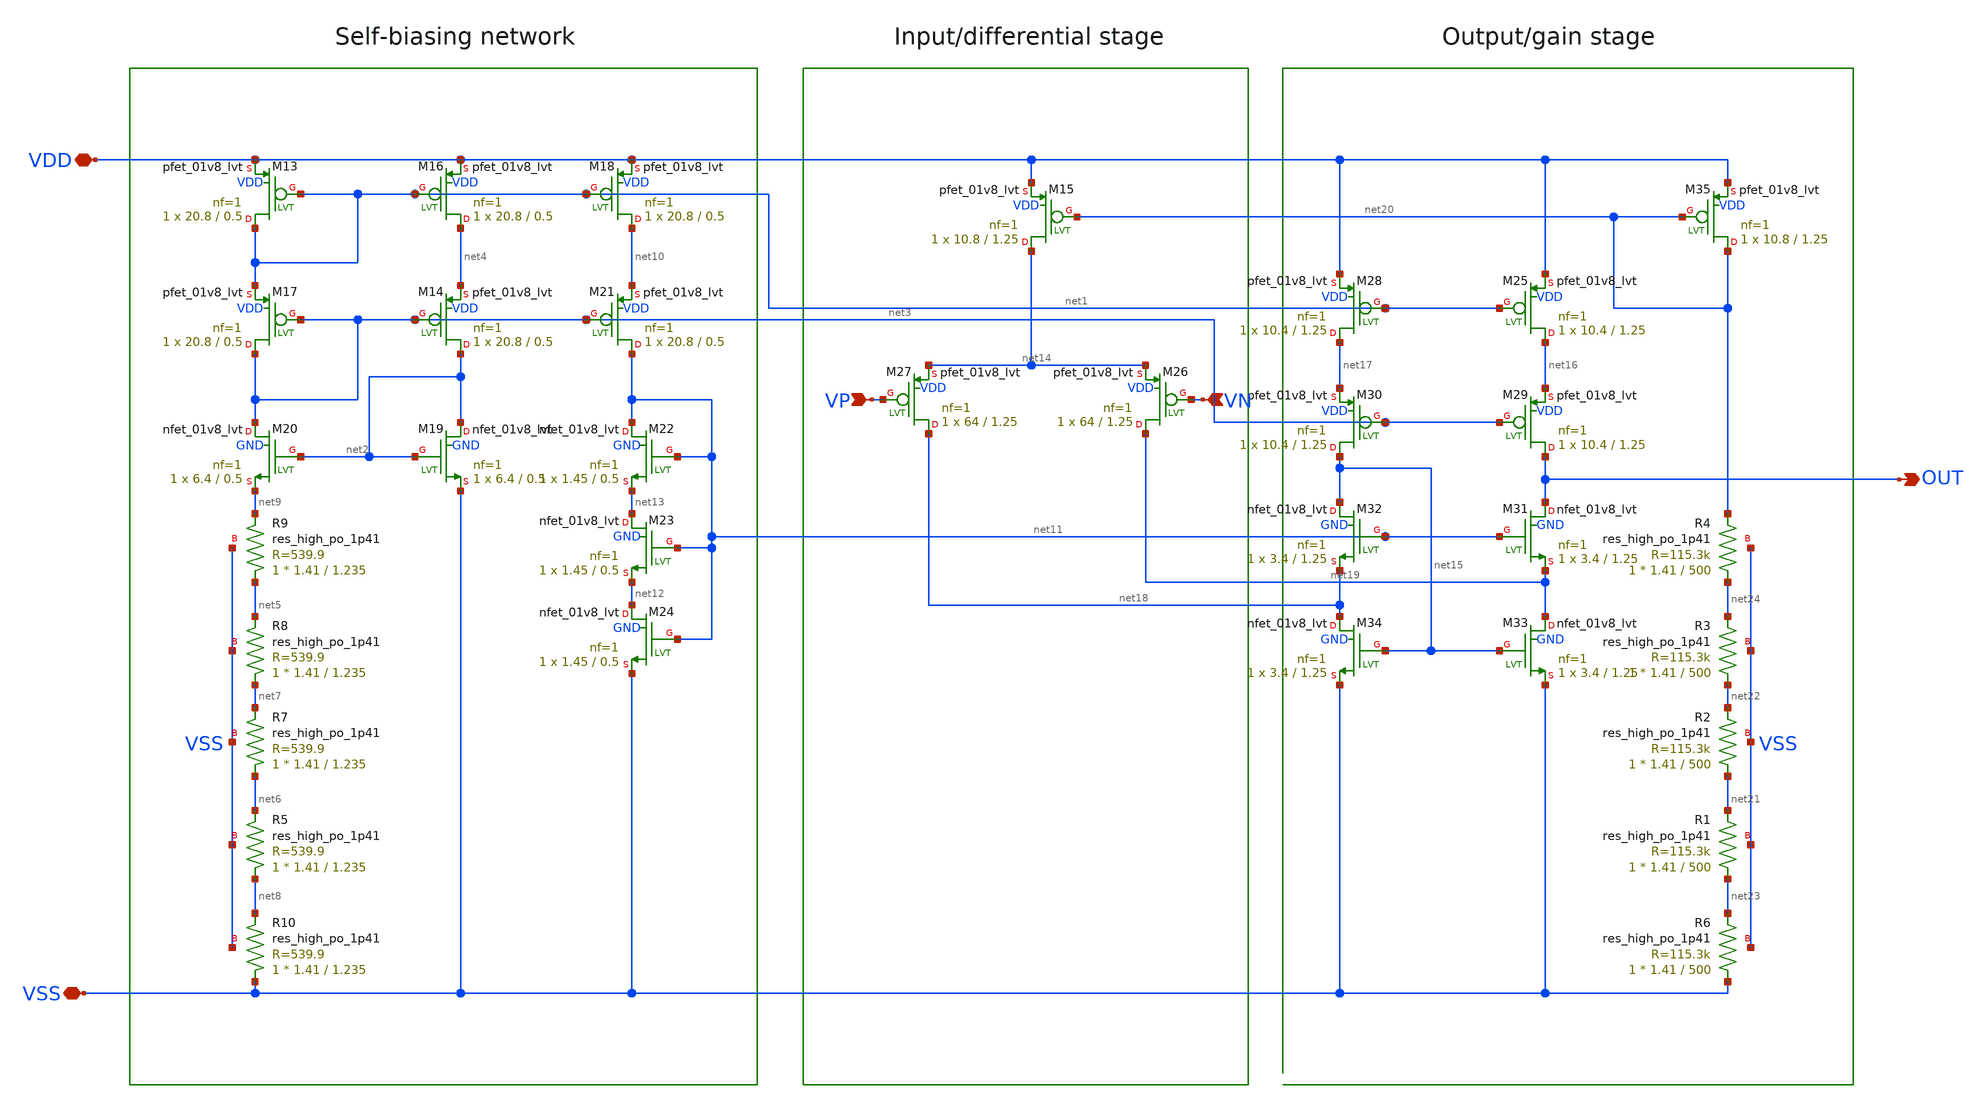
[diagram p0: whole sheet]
** sch_path: bandgap/bgr-opamp2/folded-cascode-opamp.sch
**.subckt folded-cascode-opamp VSS VDD VP VN OUT
*.iopin VSS
*.iopin VDD
*.ipin VP
*.ipin VN
*.opin OUT
XR10 VSS net8 VSS sky130_fd_pr__res_high_po_1p41 L=1.235 mult=1 m=1
XM19 net2 net2 VSS GND sky130_fd_pr__nfet_01v8_lvt L=0.5 W=6.4 nf=1 ad='int((nf+1)/2) * W/nf * 0.29'
+ as='int((nf+2)/2) * W/nf * 0.29' pd='2*int((nf+1)/2) * (W/nf + 0.29)' ps='2*int((nf+2)/2) * (W/nf + 0.29)'
+ nrd='0.29 / W' nrs='0.29 / W' sa=0 sb=0 sd=0 mult=1 m=1
XM20 net3 net2 net9 GND sky130_fd_pr__nfet_01v8_lvt L=0.5 W=6.4 nf=1 ad='int((nf+1)/2) * W/nf * 0.29'
+ as='int((nf+2)/2) * W/nf * 0.29' pd='2*int((nf+1)/2) * (W/nf + 0.29)' ps='2*int((nf+2)/2) * (W/nf + 0.29)'
+ nrd='0.29 / W' nrs='0.29 / W' sa=0 sb=0 sd=0 mult=1 m=1
XM16 net4 net1 VDD VDD sky130_fd_pr__pfet_01v8_lvt L=0.5 W=20.8 nf=1 ad='int((nf+1)/2) * W/nf * 0.29'
+ as='int((nf+2)/2) * W/nf * 0.29' pd='2*int((nf+1)/2) * (W/nf + 0.29)' ps='2*int((nf+2)/2) * (W/nf + 0.29)'
+ nrd='0.29 / W' nrs='0.29 / W' sa=0 sb=0 sd=0 mult=1 m=1
XM13 net1 net1 VDD VDD sky130_fd_pr__pfet_01v8_lvt L=0.5 W=20.8 nf=1 ad='int((nf+1)/2) * W/nf * 0.29'
+ as='int((nf+2)/2) * W/nf * 0.29' pd='2*int((nf+1)/2) * (W/nf + 0.29)' ps='2*int((nf+2)/2) * (W/nf + 0.29)'
+ nrd='0.29 / W' nrs='0.29 / W' sa=0 sb=0 sd=0 mult=1 m=1
XM14 net2 net3 net4 VDD sky130_fd_pr__pfet_01v8_lvt L=0.5 W=20.8 nf=1 ad='int((nf+1)/2) * W/nf * 0.29'
+ as='int((nf+2)/2) * W/nf * 0.29' pd='2*int((nf+1)/2) * (W/nf + 0.29)' ps='2*int((nf+2)/2) * (W/nf + 0.29)'
+ nrd='0.29 / W' nrs='0.29 / W' sa=0 sb=0 sd=0 mult=1 m=1
XM17 net3 net3 net1 VDD sky130_fd_pr__pfet_01v8_lvt L=0.5 W=20.8 nf=1 ad='int((nf+1)/2) * W/nf * 0.29'
+ as='int((nf+2)/2) * W/nf * 0.29' pd='2*int((nf+1)/2) * (W/nf + 0.29)' ps='2*int((nf+2)/2) * (W/nf + 0.29)'
+ nrd='0.29 / W' nrs='0.29 / W' sa=0 sb=0 sd=0 mult=1 m=1
XM18 net10 net1 VDD VDD sky130_fd_pr__pfet_01v8_lvt L=0.5 W=20.8 nf=1 ad='int((nf+1)/2) * W/nf * 0.29'
+ as='int((nf+2)/2) * W/nf * 0.29' pd='2*int((nf+1)/2) * (W/nf + 0.29)' ps='2*int((nf+2)/2) * (W/nf + 0.29)'
+ nrd='0.29 / W' nrs='0.29 / W' sa=0 sb=0 sd=0 mult=1 m=1
XM21 net11 net3 net10 VDD sky130_fd_pr__pfet_01v8_lvt L=0.5 W=20.8 nf=1 ad='int((nf+1)/2) * W/nf * 0.29'
+ as='int((nf+2)/2) * W/nf * 0.29' pd='2*int((nf+1)/2) * (W/nf + 0.29)' ps='2*int((nf+2)/2) * (W/nf + 0.29)'
+ nrd='0.29 / W' nrs='0.29 / W' sa=0 sb=0 sd=0 mult=1 m=1
XM22 net11 net11 net13 GND sky130_fd_pr__nfet_01v8_lvt L=0.5 W=1.45 nf=1 ad='int((nf+1)/2) * W/nf * 0.29'
+ as='int((nf+2)/2) * W/nf * 0.29' pd='2*int((nf+1)/2) * (W/nf + 0.29)' ps='2*int((nf+2)/2) * (W/nf + 0.29)'
+ nrd='0.29 / W' nrs='0.29 / W' sa=0 sb=0 sd=0 mult=1 m=1
XM23 net13 net11 net12 GND sky130_fd_pr__nfet_01v8_lvt L=0.5 W=1.45 nf=1 ad='int((nf+1)/2) * W/nf * 0.29'
+ as='int((nf+2)/2) * W/nf * 0.29' pd='2*int((nf+1)/2) * (W/nf + 0.29)' ps='2*int((nf+2)/2) * (W/nf + 0.29)'
+ nrd='0.29 / W' nrs='0.29 / W' sa=0 sb=0 sd=0 mult=1 m=1
XM24 net12 net11 VSS GND sky130_fd_pr__nfet_01v8_lvt L=0.5 W=1.45 nf=1 ad='int((nf+1)/2) * W/nf * 0.29'
+ as='int((nf+2)/2) * W/nf * 0.29' pd='2*int((nf+1)/2) * (W/nf + 0.29)' ps='2*int((nf+2)/2) * (W/nf + 0.29)'
+ nrd='0.29 / W' nrs='0.29 / W' sa=0 sb=0 sd=0 mult=1 m=1
XM26 net19 VN net14 VDD sky130_fd_pr__pfet_01v8_lvt L=1.25 W=64 nf=1 ad='int((nf+1)/2) * W/nf * 0.29'
+ as='int((nf+2)/2) * W/nf * 0.29' pd='2*int((nf+1)/2) * (W/nf + 0.29)' ps='2*int((nf+2)/2) * (W/nf + 0.29)'
+ nrd='0.29 / W' nrs='0.29 / W' sa=0 sb=0 sd=0 mult=1 m=1
XM27 net18 VP net14 VDD sky130_fd_pr__pfet_01v8_lvt L=1.25 W=64 nf=1 ad='int((nf+1)/2) * W/nf * 0.29'
+ as='int((nf+2)/2) * W/nf * 0.29' pd='2*int((nf+1)/2) * (W/nf + 0.29)' ps='2*int((nf+2)/2) * (W/nf + 0.29)'
+ nrd='0.29 / W' nrs='0.29 / W' sa=0 sb=0 sd=0 mult=1 m=1
XM15 net14 net20 VDD VDD sky130_fd_pr__pfet_01v8_lvt L=1.25 W=10.8 nf=1 ad='int((nf+1)/2) * W/nf * 0.29'
+ as='int((nf+2)/2) * W/nf * 0.29' pd='2*int((nf+1)/2) * (W/nf + 0.29)' ps='2*int((nf+2)/2) * (W/nf + 0.29)'
+ nrd='0.29 / W' nrs='0.29 / W' sa=0 sb=0 sd=0 mult=1 m=1
XM25 net16 net1 VDD VDD sky130_fd_pr__pfet_01v8_lvt L=1.25 W=10.4 nf=1 ad='int((nf+1)/2) * W/nf * 0.29'
+ as='int((nf+2)/2) * W/nf * 0.29' pd='2*int((nf+1)/2) * (W/nf + 0.29)' ps='2*int((nf+2)/2) * (W/nf + 0.29)'
+ nrd='0.29 / W' nrs='0.29 / W' sa=0 sb=0 sd=0 mult=1 m=1
XM28 net17 net1 VDD VDD sky130_fd_pr__pfet_01v8_lvt L=1.25 W=10.4 nf=1 ad='int((nf+1)/2) * W/nf * 0.29'
+ as='int((nf+2)/2) * W/nf * 0.29' pd='2*int((nf+1)/2) * (W/nf + 0.29)' ps='2*int((nf+2)/2) * (W/nf + 0.29)'
+ nrd='0.29 / W' nrs='0.29 / W' sa=0 sb=0 sd=0 mult=1 m=1
XM29 OUT net3 net16 VDD sky130_fd_pr__pfet_01v8_lvt L=1.25 W=10.4 nf=1 ad='int((nf+1)/2) * W/nf * 0.29'
+ as='int((nf+2)/2) * W/nf * 0.29' pd='2*int((nf+1)/2) * (W/nf + 0.29)' ps='2*int((nf+2)/2) * (W/nf + 0.29)'
+ nrd='0.29 / W' nrs='0.29 / W' sa=0 sb=0 sd=0 mult=1 m=1
XM30 net15 net3 net17 VDD sky130_fd_pr__pfet_01v8_lvt L=1.25 W=10.4 nf=1 ad='int((nf+1)/2) * W/nf * 0.29'
+ as='int((nf+2)/2) * W/nf * 0.29' pd='2*int((nf+1)/2) * (W/nf + 0.29)' ps='2*int((nf+2)/2) * (W/nf + 0.29)'
+ nrd='0.29 / W' nrs='0.29 / W' sa=0 sb=0 sd=0 mult=1 m=1
XM31 OUT net11 net19 GND sky130_fd_pr__nfet_01v8_lvt L=1.25 W=3.4 nf=1 ad='int((nf+1)/2) * W/nf * 0.29'
+ as='int((nf+2)/2) * W/nf * 0.29' pd='2*int((nf+1)/2) * (W/nf + 0.29)' ps='2*int((nf+2)/2) * (W/nf + 0.29)'
+ nrd='0.29 / W' nrs='0.29 / W' sa=0 sb=0 sd=0 mult=1 m=1
XM32 net15 net11 net18 GND sky130_fd_pr__nfet_01v8_lvt L=1.25 W=3.4 nf=1 ad='int((nf+1)/2) * W/nf * 0.29'
+ as='int((nf+2)/2) * W/nf * 0.29' pd='2*int((nf+1)/2) * (W/nf + 0.29)' ps='2*int((nf+2)/2) * (W/nf + 0.29)'
+ nrd='0.29 / W' nrs='0.29 / W' sa=0 sb=0 sd=0 mult=1 m=1
XM33 net19 net15 VSS GND sky130_fd_pr__nfet_01v8_lvt L=1.25 W=3.4 nf=1 ad='int((nf+1)/2) * W/nf * 0.29'
+ as='int((nf+2)/2) * W/nf * 0.29' pd='2*int((nf+1)/2) * (W/nf + 0.29)' ps='2*int((nf+2)/2) * (W/nf + 0.29)'
+ nrd='0.29 / W' nrs='0.29 / W' sa=0 sb=0 sd=0 mult=1 m=1
XM34 net18 net15 VSS GND sky130_fd_pr__nfet_01v8_lvt L=1.25 W=3.4 nf=1 ad='int((nf+1)/2) * W/nf * 0.29'
+ as='int((nf+2)/2) * W/nf * 0.29' pd='2*int((nf+1)/2) * (W/nf + 0.29)' ps='2*int((nf+2)/2) * (W/nf + 0.29)'
+ nrd='0.29 / W' nrs='0.29 / W' sa=0 sb=0 sd=0 mult=1 m=1
XM35 net20 net20 VDD VDD sky130_fd_pr__pfet_01v8_lvt L=1.25 W=10.8 nf=1 ad='int((nf+1)/2) * W/nf * 0.29'
+ as='int((nf+2)/2) * W/nf * 0.29' pd='2*int((nf+1)/2) * (W/nf + 0.29)' ps='2*int((nf+2)/2) * (W/nf + 0.29)'
+ nrd='0.29 / W' nrs='0.29 / W' sa=0 sb=0 sd=0 mult=1 m=1
XR6 VSS net23 VSS sky130_fd_pr__res_high_po_1p41 L=500 mult=1 m=1
XR1 net23 net21 VSS sky130_fd_pr__res_high_po_1p41 L=500 mult=1 m=1
XR2 net21 net22 VSS sky130_fd_pr__res_high_po_1p41 L=500 mult=1 m=1
XR3 net22 net24 VSS sky130_fd_pr__res_high_po_1p41 L=500 mult=1 m=1
XR4 net24 net20 VSS sky130_fd_pr__res_high_po_1p41 L=500 mult=1 m=1
XR5 net8 net6 VSS sky130_fd_pr__res_high_po_1p41 L=1.235 mult=1 m=1
XR7 net6 net7 VSS sky130_fd_pr__res_high_po_1p41 L=1.235 mult=1 m=1
XR8 net7 net5 VSS sky130_fd_pr__res_high_po_1p41 L=1.235 mult=1 m=1
XR9 net5 net9 VSS sky130_fd_pr__res_high_po_1p41 L=1.235 mult=1 m=1
**.ends
.end
